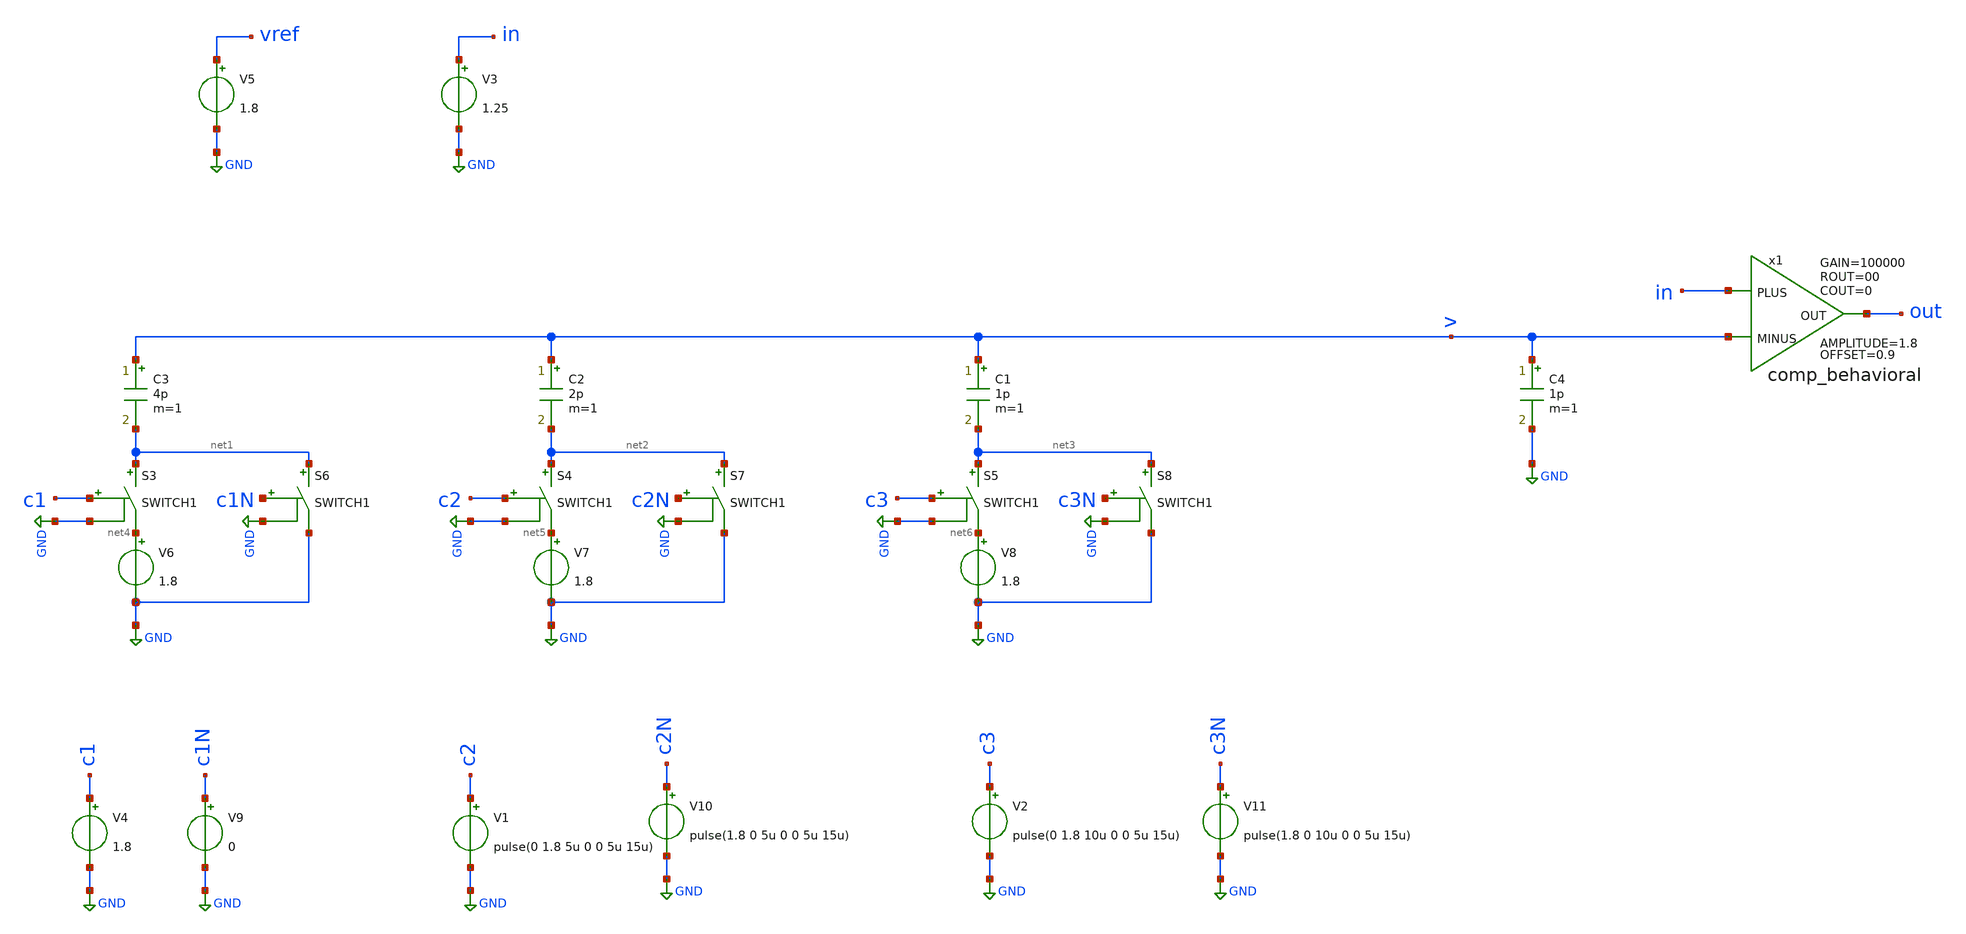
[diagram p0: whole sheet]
** sch_path: Behavioral_model/two_charge_discharge.sch
**.subckt two_charge_discharge
x1 in v out comp_behavioral OFFSET=0.9 AMPLITUDE=1.8 GAIN=100000 ROUT=00 COUT=0
V3 in GND 1.25
V4 c1 GND 1.8
C1 v net3 1p m=1
C2 v net2 2p m=1
C3 v net1 4p m=1
C4 v GND 1p m=1
V1 c2 GND pulse(0 1.8 5u 0 0 5u 15u)
V2 c3 GND pulse(0 1.8 10u 0 0 5u 15u)
V5 vref GND 1.8
S3 net1 net4 c1 GND SWITCH1
V6 net4 GND 1.8
S4 net2 net5 c2 GND SWITCH1
V7 net5 GND 1.8
S5 net3 net6 c3 GND SWITCH1
V8 net6 GND 1.8
S6 net1 GND c1N GND SWITCH1
V9 c1N GND 0
S7 net2 GND c2N GND SWITCH1
V10 c2N GND pulse(1.8 0 5u 0 0 5u 15u)
S8 net3 GND c3N GND SWITCH1
V11 c3N GND pulse(1.8 0 10u 0 0 5u 15u)
**** begin user architecture code

.tran 1n 15u
.save all
.control
plot c1; plot c2; plot c3; plot V
.endc


.lib /usr/local/share/pdk/sky130A/libs.tech/ngspice/sky130.lib.spice tt


.model switch1 sw vt=0.1 vh=0 ron=1m roff=100G

**** end user architecture code
**.ends

* expanding   symbol:  comp_behavioral.sym # of pins=3
** sym_path: Behavioral_model/comp_behavioral.sym
** sch_path: Behavioral_model/comp_behavioral.sch
.subckt comp_behavioral PLUS MINUS OUT  OFFSET=0.9 AMPLITUDE=0.9 GAIN=100000 ROUT=00 COUT=0
*.ipin PLUS
*.ipin MINUS
*.opin OUT
B1 IOUT 0 V = {OFFSET + AMPLITUDE/2*(tanh(V(IPLUS,IMINUS)*GAIN*2/AMPLITUDE))}
V1 IPLUS PLUS 3
V2 IMINUS MINUS 3
R1 OUT IOUT {ROUT} m=1
C3 OUT 0 {COUT} m=1
.ends

.GLOBAL GND
.end
